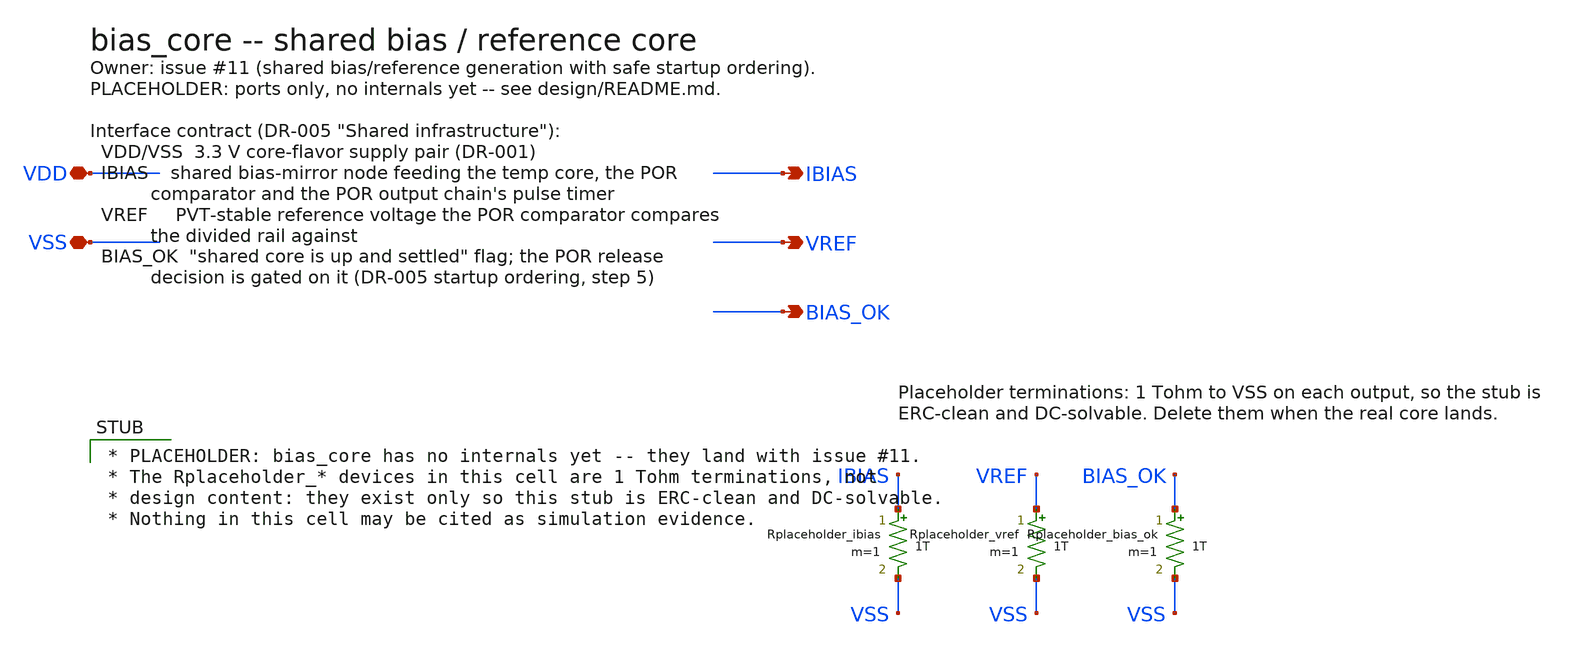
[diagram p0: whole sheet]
** sch_path: design/bias_core.sch
**.subckt bias_core VDD VSS IBIAS VREF BIAS_OK
*.iopin VDD
*.iopin VSS
*.opin IBIAS
*.opin VREF
*.opin BIAS_OK
Rplaceholder_ibias IBIAS VSS 1T m=1
Rplaceholder_vref VREF VSS 1T m=1
Rplaceholder_bias_ok BIAS_OK VSS 1T m=1
**** begin user architecture code

* PLACEHOLDER: bias_core has no internals yet -- they land with issue #11.
* The Rplaceholder_* devices in this cell are 1 Tohm terminations, not
* design content: they exist only so this stub is ERC-clean and DC-solvable.
* Nothing in this cell may be cited as simulation evidence.

**** end user architecture code
**.ends
.end
